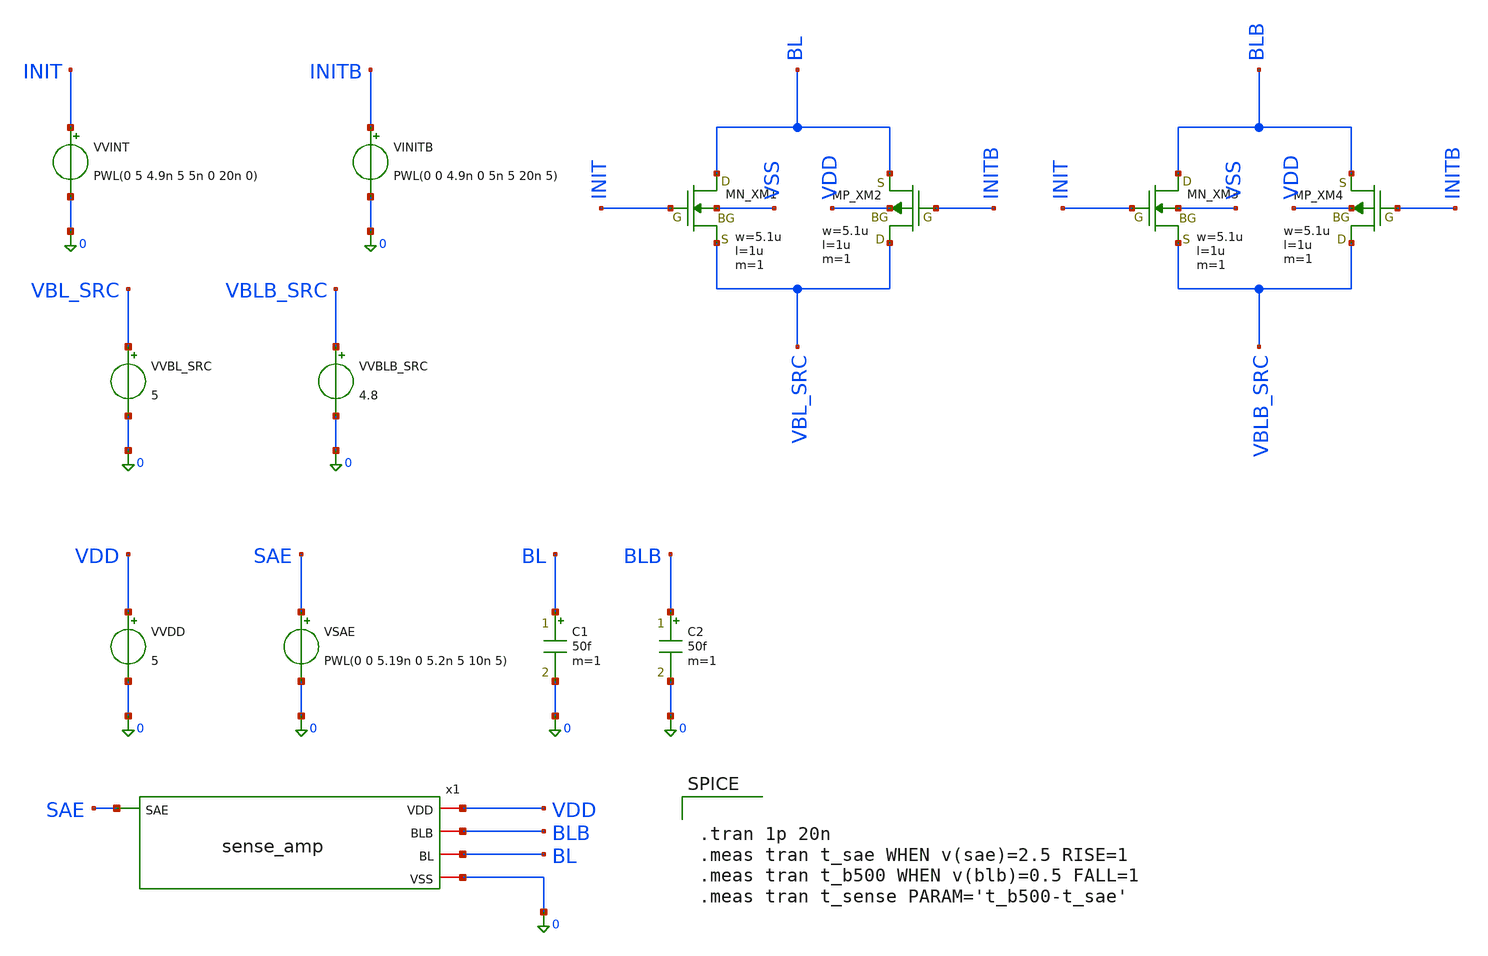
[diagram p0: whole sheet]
** sch_path: cell/tb_sense_amp_sensitivity.sch
**.subckt tb_sense_amp_sensitivity
x1 VDD BLB BL SAE 0 sense_amp
VVDD VDD 0 5
VSAE SAE 0 PWL(0 0 5.19n 0 5.2n 5 10n 5)
C1 BL 0 50f m=1
C2 BLB 0 50f m=1
VVBL_SRC VBL_SRC 0 5
VVBLB_SRC VBLB_SRC 0 4.8
XXM1 BL INIT VBL_SRC VSS NMOS w=5.1u l=1u nrd=0 nrs=0 m=1
XXM2 VBL_SRC INITB BL VDD PMOS w=5.1u l=1u nrd=0 nrs=0 m=1
XXM3 BLB INIT VBLB_SRC VSS NMOS w=5.1u l=1u nrd=0 nrs=0 m=1
XXM4 VBLB_SRC INITB BLB VDD PMOS w=5.1u l=1u nrd=0 nrs=0 m=1
VVINT INIT 0 PWL(0 5 4.9n 5 5n 0 20n 0)
VINITB INITB 0 PWL(0 0 4.9n 0 5n 5 20n 5)
**** begin user architecture code


.tran 1p 20n
.meas tran t_sae WHEN v(sae)=2.5 RISE=1
.meas tran t_b500 WHEN v(blb)=0.5 FALL=1
.meas tran t_sense PARAM='t_b500-t_sae'


 .include $::LIB/ip62_models
**** end user architecture code
**.ends
.end
